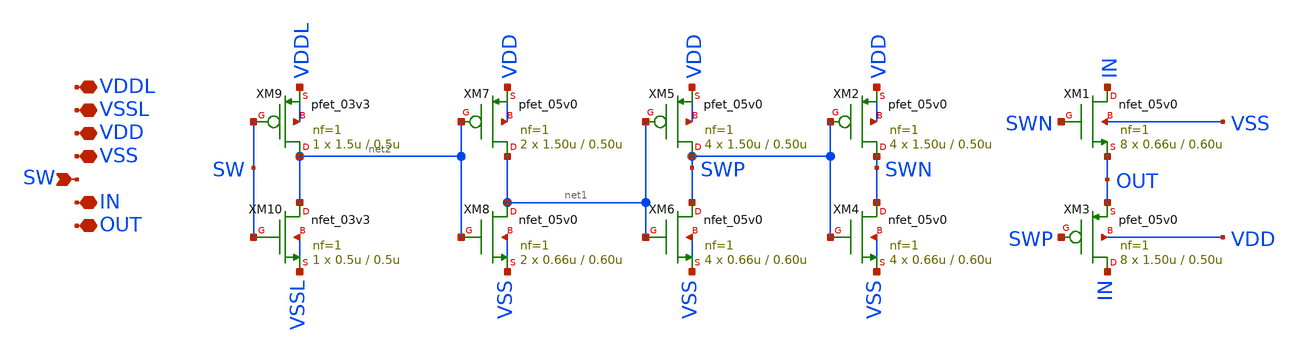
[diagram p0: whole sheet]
** sch_path: xschem/switch-matrix/transmission_gate.sch
**.subckt transmission_gate VDD VSS IN OUT SW VDDL VSSL
*.iopin VDD
*.iopin VSS
*.iopin IN
*.iopin OUT
*.ipin SW
*.iopin VDDL
*.iopin VSSL
XM3 IN SWP OUT VDD pfet_05v0 L=0.50u W=1.50u nf=1 ad='int((nf+1)/2) * W/nf * 0.18u' as='int((nf+2)/2) * W/nf * 0.18u'
+ pd='2*int((nf+1)/2) * (W/nf + 0.18u)' ps='2*int((nf+2)/2) * (W/nf + 0.18u)' nrd='0.18u / W' nrs='0.18u / W'
+ sa=0 sb=0 sd=0 m=8
XM1 IN SWN OUT VSS nfet_05v0 L=0.60u W=0.66u nf=1 ad='int((nf+1)/2) * W/nf * 0.18u' as='int((nf+2)/2) * W/nf * 0.18u'
+ pd='2*int((nf+1)/2) * (W/nf + 0.18u)' ps='2*int((nf+2)/2) * (W/nf + 0.18u)' nrd='0.18u / W' nrs='0.18u / W'
+ sa=0 sb=0 sd=0 m=8
XM2 SWN SWP VDD VDD pfet_05v0 L=0.50u W=1.50u nf=1 ad='int((nf+1)/2) * W/nf * 0.18u' as='int((nf+2)/2) * W/nf * 0.18u'
+ pd='2*int((nf+1)/2) * (W/nf + 0.18u)' ps='2*int((nf+2)/2) * (W/nf + 0.18u)' nrd='0.18u / W' nrs='0.18u / W'
+ sa=0 sb=0 sd=0 m=4
XM4 SWN SWP VSS VSS nfet_05v0 L=0.60u W=0.66u nf=1 ad='int((nf+1)/2) * W/nf * 0.18u' as='int((nf+2)/2) * W/nf * 0.18u'
+ pd='2*int((nf+1)/2) * (W/nf + 0.18u)' ps='2*int((nf+2)/2) * (W/nf + 0.18u)' nrd='0.18u / W' nrs='0.18u / W'
+ sa=0 sb=0 sd=0 m=4
XM5 SWP net1 VDD VDD pfet_05v0 L=0.50u W=1.50u nf=1 ad='int((nf+1)/2) * W/nf * 0.18u' as='int((nf+2)/2) * W/nf * 0.18u'
+ pd='2*int((nf+1)/2) * (W/nf + 0.18u)' ps='2*int((nf+2)/2) * (W/nf + 0.18u)' nrd='0.18u / W' nrs='0.18u / W'
+ sa=0 sb=0 sd=0 m=4
XM6 SWP net1 VSS VSS nfet_05v0 L=0.60u W=0.66u nf=1 ad='int((nf+1)/2) * W/nf * 0.18u' as='int((nf+2)/2) * W/nf * 0.18u'
+ pd='2*int((nf+1)/2) * (W/nf + 0.18u)' ps='2*int((nf+2)/2) * (W/nf + 0.18u)' nrd='0.18u / W' nrs='0.18u / W'
+ sa=0 sb=0 sd=0 m=4
XM7 net1 net2 VDD VDD pfet_05v0 L=0.50u W=1.50u nf=1 ad='int((nf+1)/2) * W/nf * 0.18u' as='int((nf+2)/2) * W/nf * 0.18u'
+ pd='2*int((nf+1)/2) * (W/nf + 0.18u)' ps='2*int((nf+2)/2) * (W/nf + 0.18u)' nrd='0.18u / W' nrs='0.18u / W'
+ sa=0 sb=0 sd=0 m=2
XM8 net1 net2 VSS VSS nfet_05v0 L=0.60u W=0.66u nf=1 ad='int((nf+1)/2) * W/nf * 0.18u' as='int((nf+2)/2) * W/nf * 0.18u'
+ pd='2*int((nf+1)/2) * (W/nf + 0.18u)' ps='2*int((nf+2)/2) * (W/nf + 0.18u)' nrd='0.18u / W' nrs='0.18u / W'
+ sa=0 sb=0 sd=0 m=2
XM9 net2 SW VDDL VDDL pfet_03v3 L=0.5u W=1.5u nf=1 ad='int((nf+1)/2) * W/nf * 0.18u' as='int((nf+2)/2) * W/nf * 0.18u'
+ pd='2*int((nf+1)/2) * (W/nf + 0.18u)' ps='2*int((nf+2)/2) * (W/nf + 0.18u)' nrd='0.18u / W' nrs='0.18u / W'
+ sa=0 sb=0 sd=0 m=1
XM10 net2 SW VSSL VSSL nfet_03v3 L=0.5u W=0.5u nf=1 ad='int((nf+1)/2) * W/nf * 0.18u' as='int((nf+2)/2) * W/nf * 0.18u'
+ pd='2*int((nf+1)/2) * (W/nf + 0.18u)' ps='2*int((nf+2)/2) * (W/nf + 0.18u)' nrd='0.18u / W' nrs='0.18u / W'
+ sa=0 sb=0 sd=0 m=1
**.ends
.end
